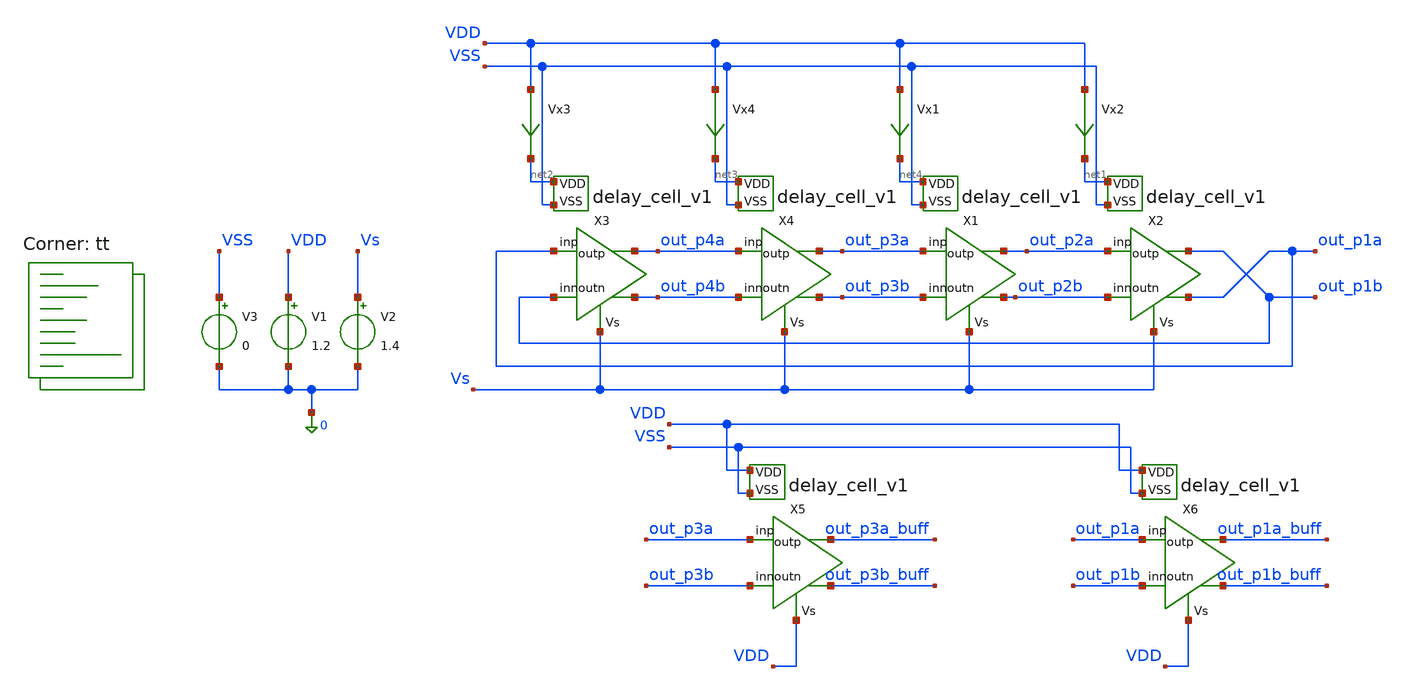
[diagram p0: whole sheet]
** sch_path: src/delay_cell_tb.sch
**.subckt delay_cell_tb
X1 net4 out_p2b out_p2a out_p3a out_p3b Vs VSS delay_cell_v1
X2 net1 out_p1a out_p1b out_p2a out_p2b Vs VSS delay_cell_v1
V1 VDD 0 1.2
.save i(v1)
V2 Vs 0 1.4
.save i(v2)
V3 VSS 0 0
.save i(v3)
X3 net2 out_p4b out_p4a out_p1a out_p1b Vs VSS delay_cell_v1
X4 net3 out_p3b out_p3a out_p4a out_p4b Vs VSS delay_cell_v1
X5 VDD out_p3b_buff out_p3a_buff out_p3a out_p3b VDD VSS delay_cell_v1
X6 VDD out_p1b_buff out_p1a_buff out_p1a out_p1b VDD VSS delay_cell_v1
Vx1 VDD net4 0
.save i(vx1)
Vx2 VDD net1 0
.save i(vx2)
Vx4 VDD net3 0
.save i(vx4)
Vx3 VDD net2 0
.save i(vx3)
**** begin user architecture code
.lib $::SKYWATER_MODELS/sky130.lib.spice tt


.option savecurrents method=gear
.save all
.control
  tran 0.01n 10n
  remzerovec
  write delay_cell_tb.raw
.endc


**** end user architecture code
**.ends

* expanding   symbol:  /home/nebk/Documents/electronics/sky130-sellicott-VCO/src/delay_cell_v1.sym #
*+ of pins=7
** sym_path: src/delay_cell_v1.sym
** sch_path: src/delay_cell_v1.sch
.subckt delay_cell_v1 VDD outn outp inp inn Vs VSS
*.ipin inp
*.ipin inn
*.opin outp
*.opin outn
*.ipin VDD
*.ipin VSS
*.ipin Vs
XM8 outn inp vtail VSS sky130_fd_pr__nfet_01v8_lvt L=0.15 W=4.5 nf=2 ad='int((2 + 1)/2) * 4.5 / 2 * 0.29'
+ as='int((2 + 2)/2) * 4.5 / 2 * 0.29' pd='2*int((2 + 1)/2) * (4.5 / 2 + 0.29)' ps='2*int((2 + 2)/2) * (4.5 / 2 + 0.29)'
+ nrd='0.29 / 4.5 ' nrs='0.29 / 4.5 ' sa=0 sb=0 sd=0 mult=1 m=1
XM9 outp inn vtail VSS sky130_fd_pr__nfet_01v8_lvt L=0.15 W=4.5 nf=2 ad='int((2 + 1)/2) * 4.5 / 2 * 0.29'
+ as='int((2 + 2)/2) * 4.5 / 2 * 0.29' pd='2*int((2 + 1)/2) * (4.5 / 2 + 0.29)' ps='2*int((2 + 2)/2) * (4.5 / 2 + 0.29)'
+ nrd='0.29 / 4.5 ' nrs='0.29 / 4.5 ' sa=0 sb=0 sd=0 mult=1 m=1
XM7 vtail Vs VSS VSS sky130_fd_pr__nfet_01v8_lvt L=0.15 W=20 nf=10 ad='int((10 + 1)/2) * 20 / 10 * 0.29'
+ as='int((10 + 2)/2) * 20 / 10 * 0.29' pd='2*int((10 + 1)/2) * (20 / 10 + 0.29)' ps='2*int((10 + 2)/2) * (20 / 10 + 0.29)'
+ nrd='0.29 / 20 ' nrs='0.29 / 20 ' sa=0 sb=0 sd=0 mult=1 m=1
XM3 outp outp VDD VDD sky130_fd_pr__pfet_01v8_lvt L=0.35 W=9 nf=4 ad='int((4 + 1)/2) * 9 / 4 * 0.29'
+ as='int((4 + 2)/2) * 9 / 4 * 0.29' pd='2*int((4 + 1)/2) * (9 / 4 + 0.29)' ps='2*int((4 + 2)/2) * (9 / 4 + 0.29)'
+ nrd='0.29 / 9 ' nrs='0.29 / 9 ' sa=0 sb=0 sd=0 mult=1 m=1
XM2 outn outn VDD VDD sky130_fd_pr__pfet_01v8_lvt L=0.35 W=9 nf=4 ad='int((4 + 1)/2) * 9 / 4 * 0.29'
+ as='int((4 + 2)/2) * 9 / 4 * 0.29' pd='2*int((4 + 1)/2) * (9 / 4 + 0.29)' ps='2*int((4 + 2)/2) * (9 / 4 + 0.29)'
+ nrd='0.29 / 9 ' nrs='0.29 / 9 ' sa=0 sb=0 sd=0 mult=1 m=1
XM1 outn outp VDD VDD sky130_fd_pr__pfet_01v8_lvt L=0.35 W=8 nf=4 ad='int((4 + 1)/2) * 8 / 4 * 0.29'
+ as='int((4 + 2)/2) * 8 / 4 * 0.29' pd='2*int((4 + 1)/2) * (8 / 4 + 0.29)' ps='2*int((4 + 2)/2) * (8 / 4 + 0.29)'
+ nrd='0.29 / 8 ' nrs='0.29 / 8 ' sa=0 sb=0 sd=0 mult=1 m=1
XM4 outp outn VDD VDD sky130_fd_pr__pfet_01v8_lvt L=0.35 W=8 nf=4 ad='int((4 + 1)/2) * 8 / 4 * 0.29'
+ as='int((4 + 2)/2) * 8 / 4 * 0.29' pd='2*int((4 + 1)/2) * (8 / 4 + 0.29)' ps='2*int((4 + 2)/2) * (8 / 4 + 0.29)'
+ nrd='0.29 / 8 ' nrs='0.29 / 8 ' sa=0 sb=0 sd=0 mult=1 m=1
.ends

.end
